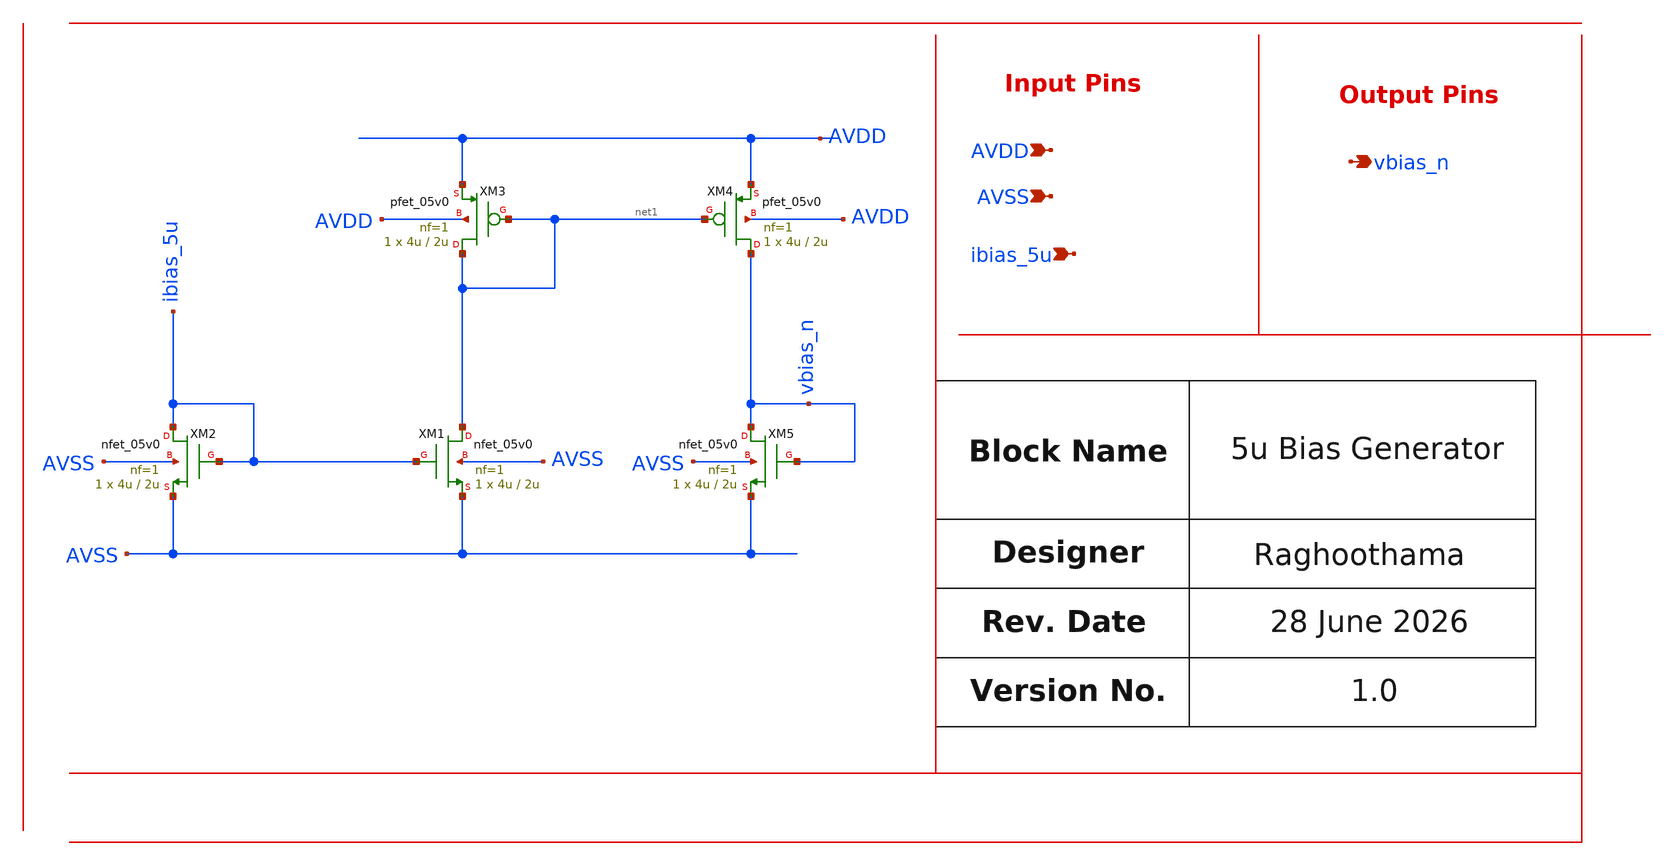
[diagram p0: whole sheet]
** sch_path: design/schematics/ADC/Adder/OTA/rrao_cic_bms_afe_iadc_biasing_ckt.sch
**.subckt rrao_cic_bms_afe_iadc_biasing_ckt AVSS AVDD vbias_n ibias_5u
*.ipin AVSS
*.ipin AVDD
*.opin vbias_n
*.ipin ibias_5u
XM1 net1 ibias_5u AVSS AVSS nfet_05v0 L=2u W=4u nf=1 ad='int((nf+1)/2) * W/nf * 0.18u' as='int((nf+2)/2) * W/nf * 0.18u'
+ pd='2*int((nf+1)/2) * (W/nf + 0.18u)' ps='2*int((nf+2)/2) * (W/nf + 0.18u)' nrd='0.18u / W' nrs='0.18u / W'
+ sa=0 sb=0 sd=0 m=1
XM3 net1 net1 AVDD AVDD pfet_05v0 L=2u W=4u nf=1 ad='int((nf+1)/2) * W/nf * 0.18u' as='int((nf+2)/2) * W/nf * 0.18u'
+ pd='2*int((nf+1)/2) * (W/nf + 0.18u)' ps='2*int((nf+2)/2) * (W/nf + 0.18u)' nrd='0.18u / W' nrs='0.18u / W'
+ sa=0 sb=0 sd=0 m=1
XM4 vbias_n net1 AVDD AVDD pfet_05v0 L=2u W=4u nf=1 ad='int((nf+1)/2) * W/nf * 0.18u' as='int((nf+2)/2) * W/nf * 0.18u'
+ pd='2*int((nf+1)/2) * (W/nf + 0.18u)' ps='2*int((nf+2)/2) * (W/nf + 0.18u)' nrd='0.18u / W' nrs='0.18u / W'
+ sa=0 sb=0 sd=0 m=1
XM5 vbias_n vbias_n AVSS AVSS nfet_05v0 L=2u W=4u nf=1 ad='int((nf+1)/2) * W/nf * 0.18u' as='int((nf+2)/2) * W/nf * 0.18u'
+ pd='2*int((nf+1)/2) * (W/nf + 0.18u)' ps='2*int((nf+2)/2) * (W/nf + 0.18u)' nrd='0.18u / W' nrs='0.18u / W'
+ sa=0 sb=0 sd=0 m=1
XM2 ibias_5u ibias_5u AVSS AVSS nfet_05v0 L=2u W=4u nf=1 ad='int((nf+1)/2) * W/nf * 0.18u' as='int((nf+2)/2) * W/nf * 0.18u'
+ pd='2*int((nf+1)/2) * (W/nf + 0.18u)' ps='2*int((nf+2)/2) * (W/nf + 0.18u)' nrd='0.18u / W' nrs='0.18u / W'
+ sa=0 sb=0 sd=0 m=1
**.ends
.end
